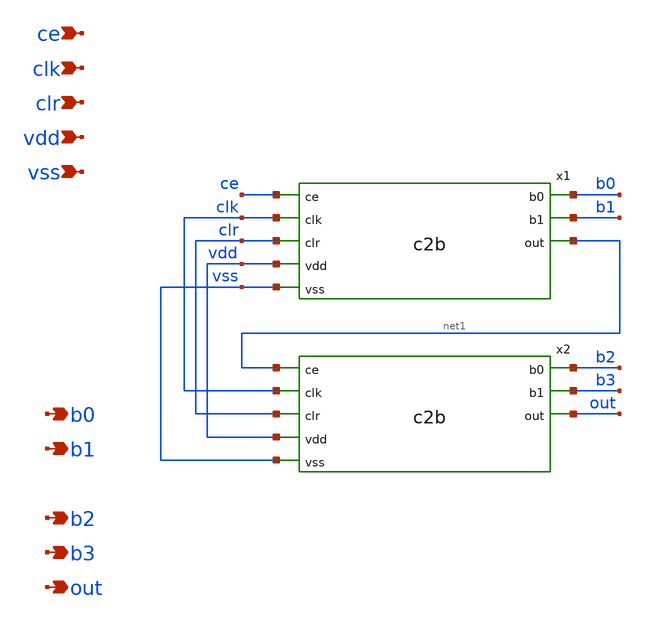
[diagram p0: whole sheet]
** sch_path: xschem/c4b.sch
**.subckt c4b clr vdd vss clk ce b1 b0 b2 b3 out
*.ipin clr
*.ipin vdd
*.ipin vss
*.ipin clk
*.ipin ce
*.opin b1
*.opin b0
*.opin b2
*.opin b3
*.opin out
x1 ce clk clr vdd vss b0 b1 net1 c2b
x2 net1 clk clr vdd vss b2 b3 out c2b
**.ends
.end
